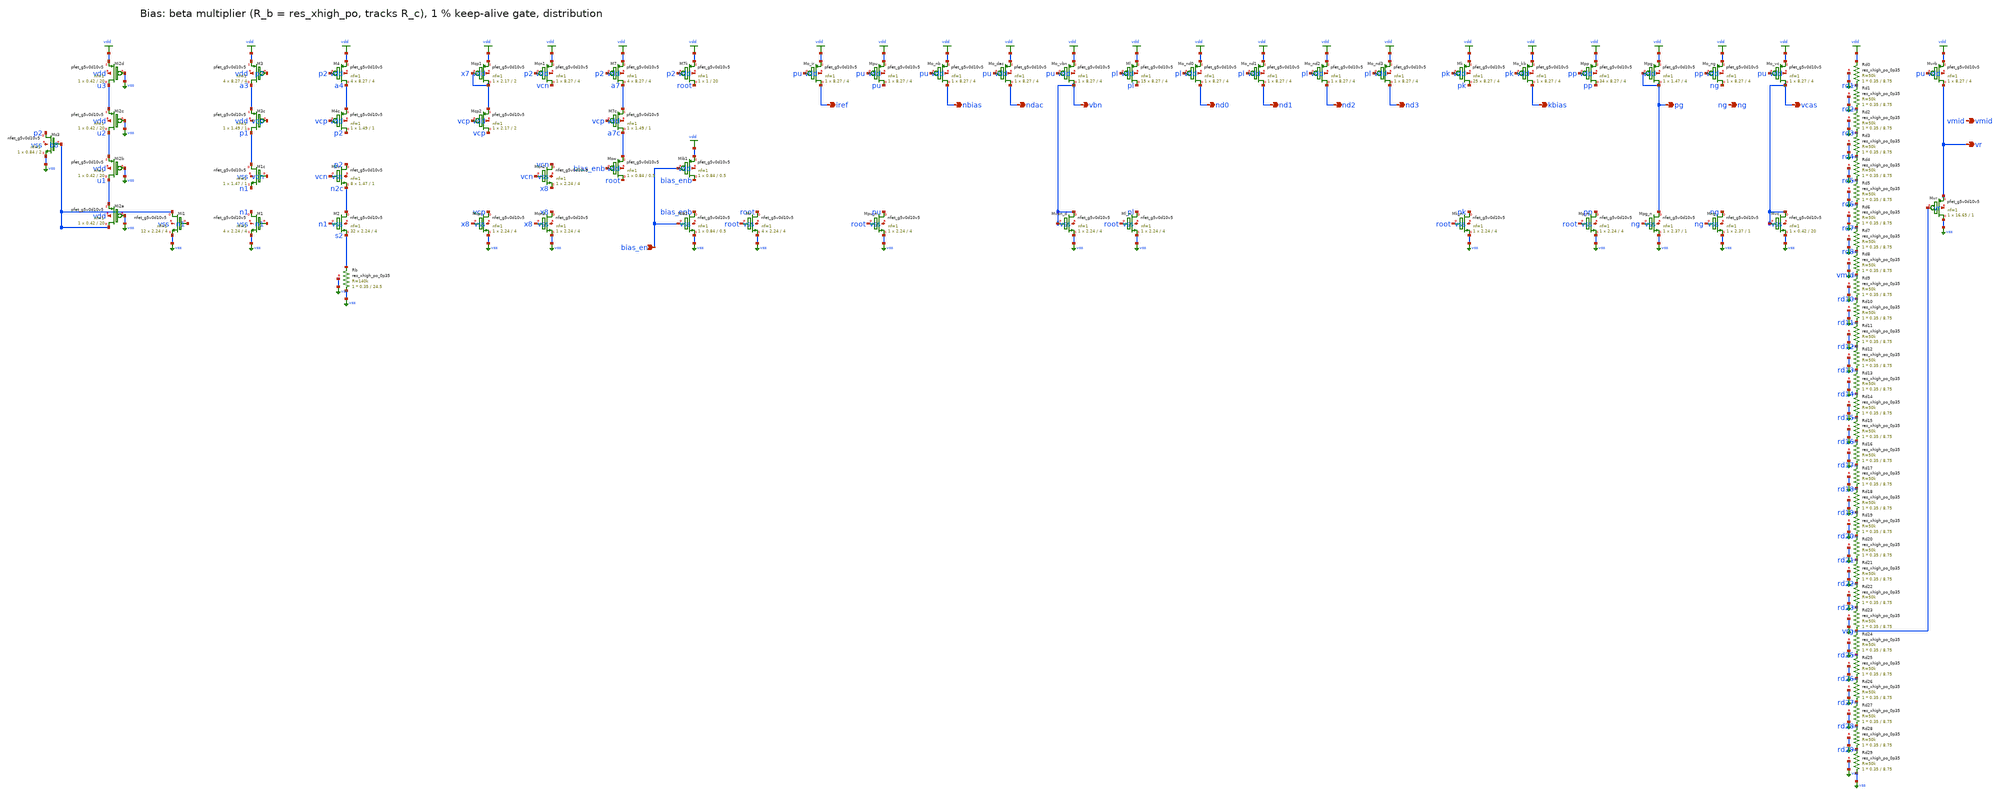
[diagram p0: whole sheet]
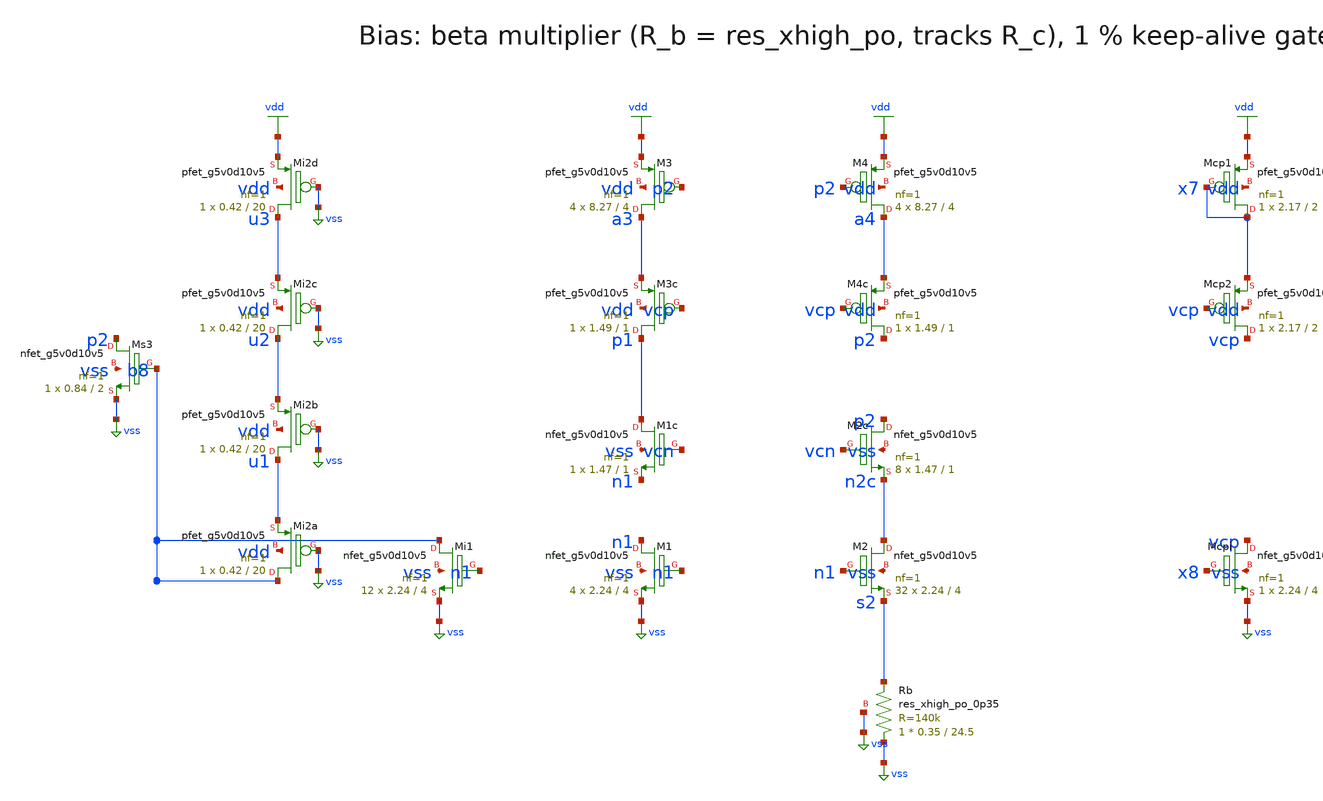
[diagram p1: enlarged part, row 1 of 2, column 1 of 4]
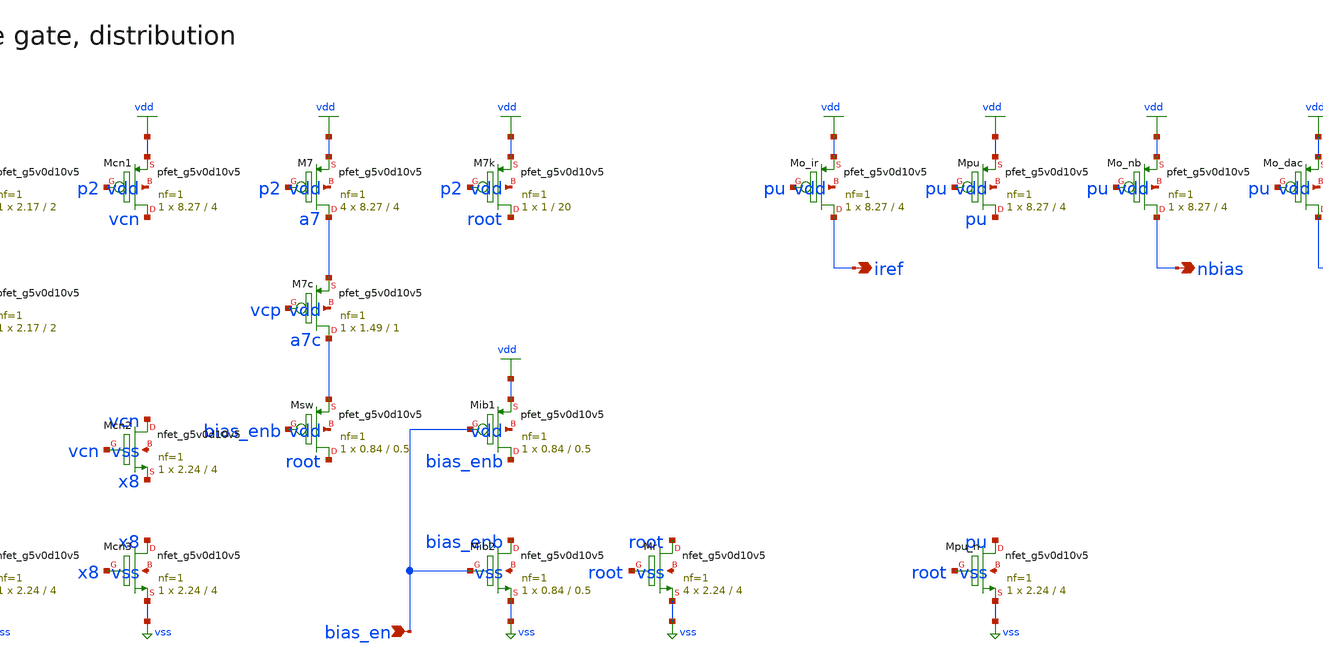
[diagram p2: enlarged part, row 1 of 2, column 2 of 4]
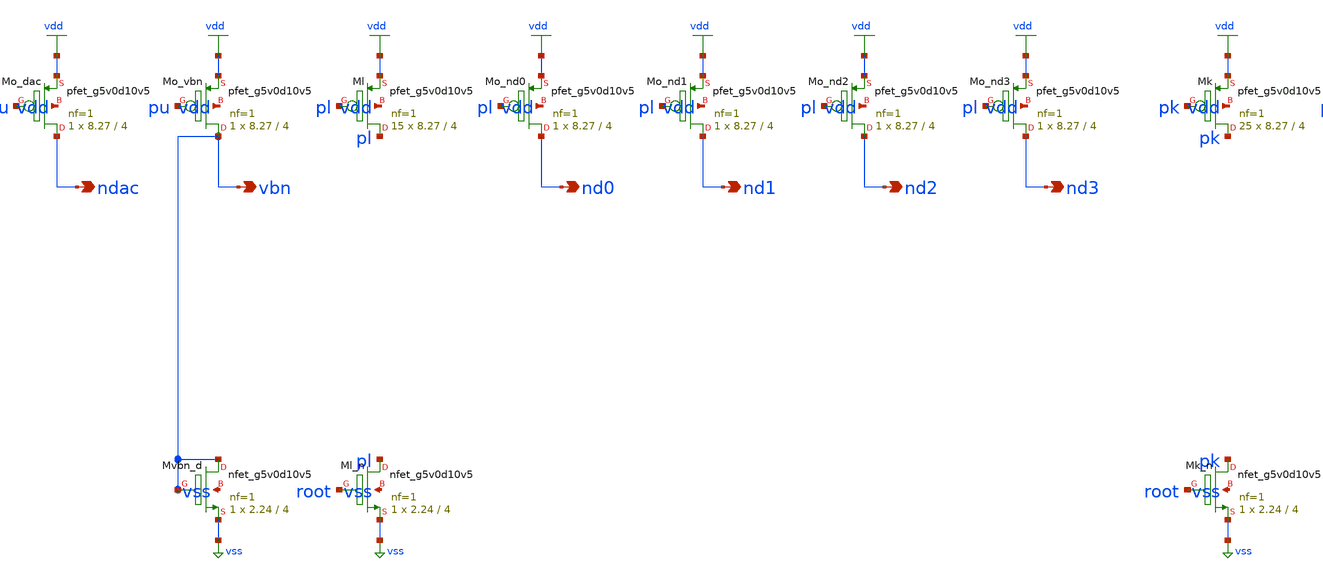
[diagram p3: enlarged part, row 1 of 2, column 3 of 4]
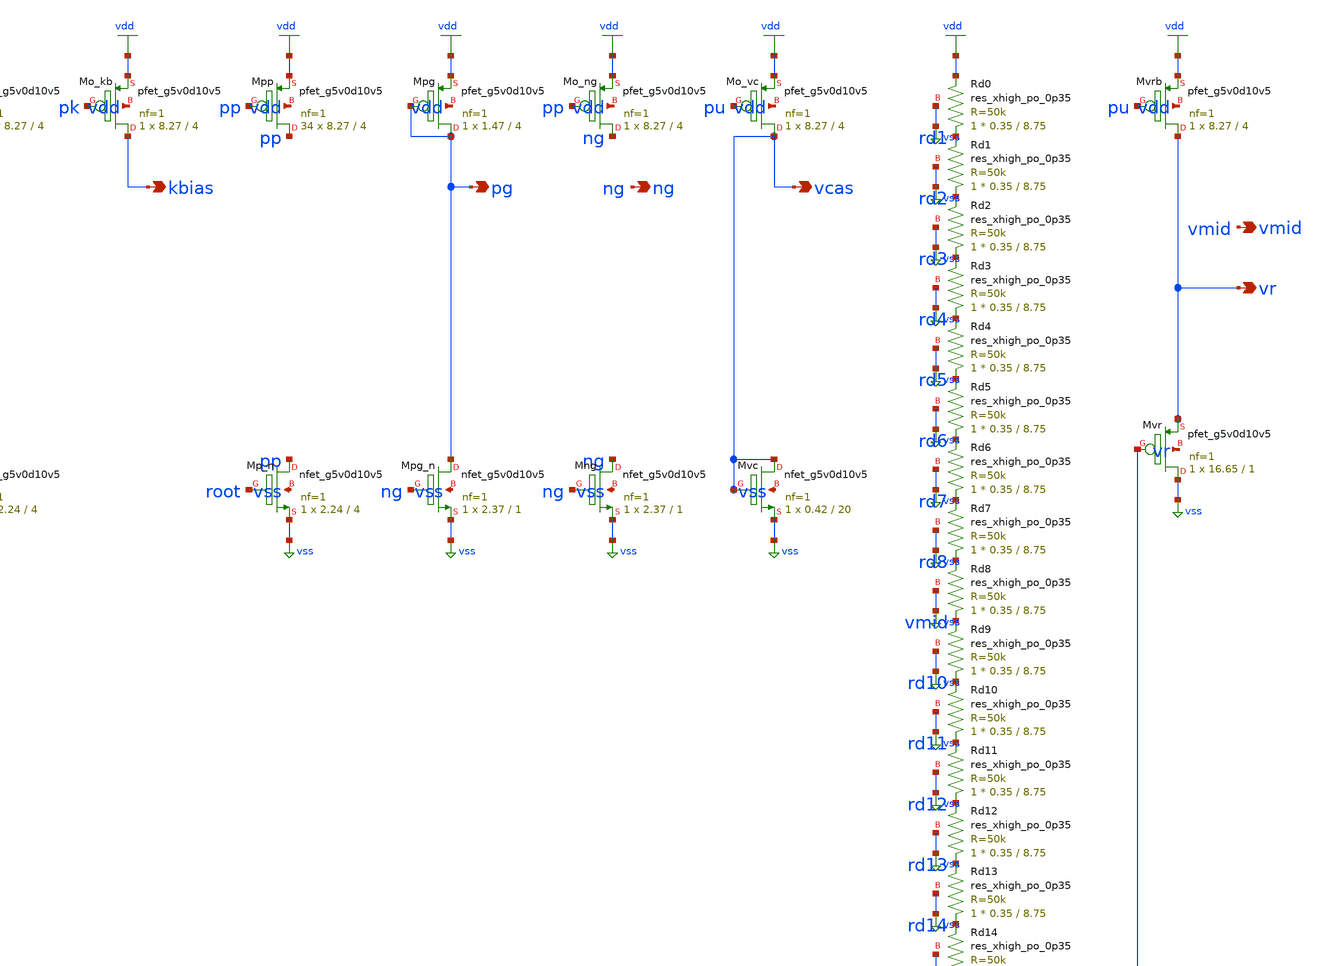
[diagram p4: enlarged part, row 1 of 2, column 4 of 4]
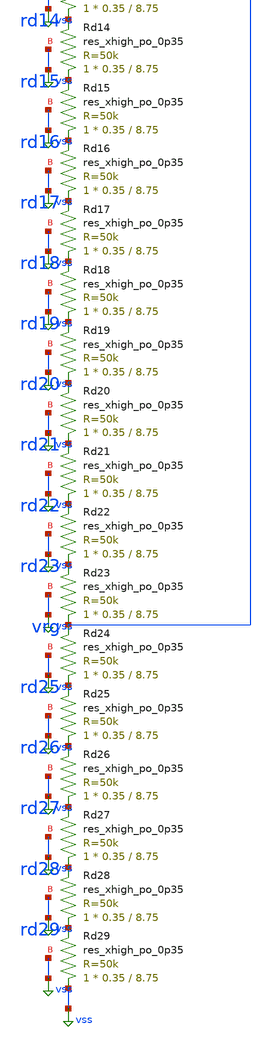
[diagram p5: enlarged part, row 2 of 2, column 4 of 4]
** sch_path: xschem/rt5w_bias.sch
**.subckt rt5w_bias bias_en nbias ndac vbn kbias pg ng vcas vr vmid iref nd0 nd1 nd2 nd3
*.ipin bias_en
*.opin nbias
*.opin ndac
*.opin vbn
*.opin kbias
*.opin pg
*.opin ng
*.opin vcas
*.opin vr
*.opin vmid
*.opin iref
*.opin nd0
*.opin nd1
*.opin nd2
*.opin nd3
XM1 n1 n1 vss vss sky130_fd_pr__nfet_g5v0d10v5 L=4 W=2.24 nf=1 ad=0.6496 as=0.6496 pd=5.06 ps=5.06
+ nrd=0.1295 nrs=0.1295 sa=0 sb=0 sd=0 mult=4 m=4
XM2 n2c n1 s2 vss sky130_fd_pr__nfet_g5v0d10v5 L=4 W=2.24 nf=1 ad=0.6496 as=0.6496 pd=5.06 ps=5.06
+ nrd=0.1295 nrs=0.1295 sa=0 sb=0 sd=0 mult=32 m=32
XRb vss s2 vss sky130_fd_pr__res_xhigh_po_0p35 L=24.5 mult=1 m=1
XM1c p1 vcn n1 vss sky130_fd_pr__nfet_g5v0d10v5 L=1 W=1.47 nf=1 ad=0.4263 as=0.4263 pd=3.52 ps=3.52
+ nrd=0.1973 nrs=0.1973 sa=0 sb=0 sd=0 mult=1 m=1
XM2c p2 vcn n2c vss sky130_fd_pr__nfet_g5v0d10v5 L=1 W=1.47 nf=1 ad=0.4263 as=0.4263 pd=3.52 ps=3.52
+ nrd=0.1973 nrs=0.1973 sa=0 sb=0 sd=0 mult=8 m=8
XM3c p1 vcp a3 vdd sky130_fd_pr__pfet_g5v0d10v5 L=1 W=1.49 nf=1 ad=0.4321 as=0.4321 pd=3.56 ps=3.56
+ nrd=0.1946 nrs=0.1946 sa=0 sb=0 sd=0 mult=1 m=1
XM4c p2 vcp a4 vdd sky130_fd_pr__pfet_g5v0d10v5 L=1 W=1.49 nf=1 ad=0.4321 as=0.4321 pd=3.56 ps=3.56
+ nrd=0.1946 nrs=0.1946 sa=0 sb=0 sd=0 mult=1 m=1
XM3 a3 p2 vdd vdd sky130_fd_pr__pfet_g5v0d10v5 L=4 W=8.27 nf=1 ad=2.398 as=2.398 pd=17.12 ps=17.12
+ nrd=0.03507 nrs=0.03507 sa=0 sb=0 sd=0 mult=4 m=4
XM4 a4 p2 vdd vdd sky130_fd_pr__pfet_g5v0d10v5 L=4 W=8.27 nf=1 ad=2.398 as=2.398 pd=17.12 ps=17.12
+ nrd=0.03507 nrs=0.03507 sa=0 sb=0 sd=0 mult=4 m=4
XMcp1 x7 x7 vdd vdd sky130_fd_pr__pfet_g5v0d10v5 L=2 W=2.17 nf=1 ad=0.6293 as=0.6293 pd=4.92 ps=4.92
+ nrd=0.1336 nrs=0.1336 sa=0 sb=0 sd=0 mult=1 m=1
XMcp2 vcp vcp x7 vdd sky130_fd_pr__pfet_g5v0d10v5 L=2 W=2.17 nf=1 ad=0.6293 as=0.6293 pd=4.92
+ ps=4.92 nrd=0.1336 nrs=0.1336 sa=0 sb=0 sd=0 mult=1 m=1
XMcpi vcp x8 vss vss sky130_fd_pr__nfet_g5v0d10v5 L=4 W=2.24 nf=1 ad=0.6496 as=0.6496 pd=5.06
+ ps=5.06 nrd=0.1295 nrs=0.1295 sa=0 sb=0 sd=0 mult=1 m=1
XMcn1 vcn p2 vdd vdd sky130_fd_pr__pfet_g5v0d10v5 L=4 W=8.27 nf=1 ad=2.398 as=2.398 pd=17.12
+ ps=17.12 nrd=0.03507 nrs=0.03507 sa=0 sb=0 sd=0 mult=1 m=1
XMcn2 vcn vcn x8 vss sky130_fd_pr__nfet_g5v0d10v5 L=4 W=2.24 nf=1 ad=0.6496 as=0.6496 pd=5.06
+ ps=5.06 nrd=0.1295 nrs=0.1295 sa=0 sb=0 sd=0 mult=1 m=1
XMcn3 x8 x8 vss vss sky130_fd_pr__nfet_g5v0d10v5 L=4 W=2.24 nf=1 ad=0.6496 as=0.6496 pd=5.06 ps=5.06
+ nrd=0.1295 nrs=0.1295 sa=0 sb=0 sd=0 mult=1 m=1
XMi1 b8 n1 vss vss sky130_fd_pr__nfet_g5v0d10v5 L=4 W=2.24 nf=1 ad=0.6496 as=0.6496 pd=5.06 ps=5.06
+ nrd=0.1295 nrs=0.1295 sa=0 sb=0 sd=0 mult=12 m=12
XMi2a b8 vss u1 vdd sky130_fd_pr__pfet_g5v0d10v5 L=20 W=0.42 nf=1 ad=0.1218 as=0.1218 pd=1.42
+ ps=1.42 nrd=0.6905 nrs=0.6905 sa=0 sb=0 sd=0 mult=1 m=1
XMi2b u1 vss u2 vdd sky130_fd_pr__pfet_g5v0d10v5 L=20 W=0.42 nf=1 ad=0.1218 as=0.1218 pd=1.42
+ ps=1.42 nrd=0.6905 nrs=0.6905 sa=0 sb=0 sd=0 mult=1 m=1
XMi2c u2 vss u3 vdd sky130_fd_pr__pfet_g5v0d10v5 L=20 W=0.42 nf=1 ad=0.1218 as=0.1218 pd=1.42
+ ps=1.42 nrd=0.6905 nrs=0.6905 sa=0 sb=0 sd=0 mult=1 m=1
XMi2d u3 vss vdd vdd sky130_fd_pr__pfet_g5v0d10v5 L=20 W=0.42 nf=1 ad=0.1218 as=0.1218 pd=1.42
+ ps=1.42 nrd=0.6905 nrs=0.6905 sa=0 sb=0 sd=0 mult=1 m=1
XMs3 p2 b8 vss vss sky130_fd_pr__nfet_g5v0d10v5 L=2 W=0.84 nf=1 ad=0.2436 as=0.2436 pd=2.26 ps=2.26
+ nrd=0.3452 nrs=0.3452 sa=0 sb=0 sd=0 mult=1 m=1
XM7 a7 p2 vdd vdd sky130_fd_pr__pfet_g5v0d10v5 L=4 W=8.27 nf=1 ad=2.398 as=2.398 pd=17.12 ps=17.12
+ nrd=0.03507 nrs=0.03507 sa=0 sb=0 sd=0 mult=4 m=4
XM7c a7c vcp a7 vdd sky130_fd_pr__pfet_g5v0d10v5 L=1 W=1.49 nf=1 ad=0.4321 as=0.4321 pd=3.56 ps=3.56
+ nrd=0.1946 nrs=0.1946 sa=0 sb=0 sd=0 mult=1 m=1
XMsw root bias_enb a7c vdd sky130_fd_pr__pfet_g5v0d10v5 L=0.5 W=0.84 nf=1 ad=0.2436 as=0.2436
+ pd=2.26 ps=2.26 nrd=0.3452 nrs=0.3452 sa=0 sb=0 sd=0 mult=1 m=1
XM7k root p2 vdd vdd sky130_fd_pr__pfet_g5v0d10v5 L=20 W=1 nf=1 ad=0.29 as=0.29 pd=2.58 ps=2.58
+ nrd=0.29 nrs=0.29 sa=0 sb=0 sd=0 mult=1 m=1
XMib1 bias_enb bias_en vdd vdd sky130_fd_pr__pfet_g5v0d10v5 L=0.5 W=0.84 nf=1 ad=0.2436 as=0.2436
+ pd=2.26 ps=2.26 nrd=0.3452 nrs=0.3452 sa=0 sb=0 sd=0 mult=1 m=1
XMib2 bias_enb bias_en vss vss sky130_fd_pr__nfet_g5v0d10v5 L=0.5 W=0.84 nf=1 ad=0.2436 as=0.2436
+ pd=2.26 ps=2.26 nrd=0.3452 nrs=0.3452 sa=0 sb=0 sd=0 mult=1 m=1
XMr root root vss vss sky130_fd_pr__nfet_g5v0d10v5 L=4 W=2.24 nf=1 ad=0.6496 as=0.6496 pd=5.06
+ ps=5.06 nrd=0.1295 nrs=0.1295 sa=0 sb=0 sd=0 mult=4 m=4
XMpu_n pu root vss vss sky130_fd_pr__nfet_g5v0d10v5 L=4 W=2.24 nf=1 ad=0.6496 as=0.6496 pd=5.06
+ ps=5.06 nrd=0.1295 nrs=0.1295 sa=0 sb=0 sd=0 mult=1 m=1
XMpu pu pu vdd vdd sky130_fd_pr__pfet_g5v0d10v5 L=4 W=8.27 nf=1 ad=2.398 as=2.398 pd=17.12 ps=17.12
+ nrd=0.03507 nrs=0.03507 sa=0 sb=0 sd=0 mult=1 m=1
XMo_nb nbias pu vdd vdd sky130_fd_pr__pfet_g5v0d10v5 L=4 W=8.27 nf=1 ad=2.398 as=2.398 pd=17.12
+ ps=17.12 nrd=0.03507 nrs=0.03507 sa=0 sb=0 sd=0 mult=1 m=1
XMo_dac ndac pu vdd vdd sky130_fd_pr__pfet_g5v0d10v5 L=4 W=8.27 nf=1 ad=2.398 as=2.398 pd=17.12
+ ps=17.12 nrd=0.03507 nrs=0.03507 sa=0 sb=0 sd=0 mult=1 m=1
XMo_ir iref pu vdd vdd sky130_fd_pr__pfet_g5v0d10v5 L=4 W=8.27 nf=1 ad=2.398 as=2.398 pd=17.12
+ ps=17.12 nrd=0.03507 nrs=0.03507 sa=0 sb=0 sd=0 mult=1 m=1
XMo_vbn vbn pu vdd vdd sky130_fd_pr__pfet_g5v0d10v5 L=4 W=8.27 nf=1 ad=2.398 as=2.398 pd=17.12
+ ps=17.12 nrd=0.03507 nrs=0.03507 sa=0 sb=0 sd=0 mult=1 m=1
XMvbn_d vbn vbn vss vss sky130_fd_pr__nfet_g5v0d10v5 L=4 W=2.24 nf=1 ad=0.6496 as=0.6496 pd=5.06
+ ps=5.06 nrd=0.1295 nrs=0.1295 sa=0 sb=0 sd=0 mult=1 m=1
XMl_n pl root vss vss sky130_fd_pr__nfet_g5v0d10v5 L=4 W=2.24 nf=1 ad=0.6496 as=0.6496 pd=5.06
+ ps=5.06 nrd=0.1295 nrs=0.1295 sa=0 sb=0 sd=0 mult=1 m=1
XMl pl pl vdd vdd sky130_fd_pr__pfet_g5v0d10v5 L=4 W=8.27 nf=1 ad=2.398 as=2.398 pd=17.12 ps=17.12
+ nrd=0.03507 nrs=0.03507 sa=0 sb=0 sd=0 mult=15 m=15
XMo_nd0 nd0 pl vdd vdd sky130_fd_pr__pfet_g5v0d10v5 L=4 W=8.27 nf=1 ad=2.398 as=2.398 pd=17.12
+ ps=17.12 nrd=0.03507 nrs=0.03507 sa=0 sb=0 sd=0 mult=1 m=1
XMo_nd1 nd1 pl vdd vdd sky130_fd_pr__pfet_g5v0d10v5 L=4 W=8.27 nf=1 ad=2.398 as=2.398 pd=17.12
+ ps=17.12 nrd=0.03507 nrs=0.03507 sa=0 sb=0 sd=0 mult=1 m=1
XMo_nd2 nd2 pl vdd vdd sky130_fd_pr__pfet_g5v0d10v5 L=4 W=8.27 nf=1 ad=2.398 as=2.398 pd=17.12
+ ps=17.12 nrd=0.03507 nrs=0.03507 sa=0 sb=0 sd=0 mult=1 m=1
XMo_nd3 nd3 pl vdd vdd sky130_fd_pr__pfet_g5v0d10v5 L=4 W=8.27 nf=1 ad=2.398 as=2.398 pd=17.12
+ ps=17.12 nrd=0.03507 nrs=0.03507 sa=0 sb=0 sd=0 mult=1 m=1
XMk_n pk root vss vss sky130_fd_pr__nfet_g5v0d10v5 L=4 W=2.24 nf=1 ad=0.6496 as=0.6496 pd=5.06
+ ps=5.06 nrd=0.1295 nrs=0.1295 sa=0 sb=0 sd=0 mult=1 m=1
XMk pk pk vdd vdd sky130_fd_pr__pfet_g5v0d10v5 L=4 W=8.27 nf=1 ad=2.398 as=2.398 pd=17.12 ps=17.12
+ nrd=0.03507 nrs=0.03507 sa=0 sb=0 sd=0 mult=25 m=25
XMo_kb kbias pk vdd vdd sky130_fd_pr__pfet_g5v0d10v5 L=4 W=8.27 nf=1 ad=2.398 as=2.398 pd=17.12
+ ps=17.12 nrd=0.03507 nrs=0.03507 sa=0 sb=0 sd=0 mult=1 m=1
XMp_n pp root vss vss sky130_fd_pr__nfet_g5v0d10v5 L=4 W=2.24 nf=1 ad=0.6496 as=0.6496 pd=5.06
+ ps=5.06 nrd=0.1295 nrs=0.1295 sa=0 sb=0 sd=0 mult=1 m=1
XMpp pp pp vdd vdd sky130_fd_pr__pfet_g5v0d10v5 L=4 W=8.27 nf=1 ad=2.398 as=2.398 pd=17.12 ps=17.12
+ nrd=0.03507 nrs=0.03507 sa=0 sb=0 sd=0 mult=34 m=34
XMpg pg pg vdd vdd sky130_fd_pr__pfet_g5v0d10v5 L=4 W=1.47 nf=1 ad=0.4263 as=0.4263 pd=3.52 ps=3.52
+ nrd=0.1973 nrs=0.1973 sa=0 sb=0 sd=0 mult=1 m=1
XMo_ng ng pp vdd vdd sky130_fd_pr__pfet_g5v0d10v5 L=4 W=8.27 nf=1 ad=2.398 as=2.398 pd=17.12
+ ps=17.12 nrd=0.03507 nrs=0.03507 sa=0 sb=0 sd=0 mult=1 m=1
XMng ng ng vss vss sky130_fd_pr__nfet_g5v0d10v5 L=1 W=2.37 nf=1 ad=0.6873 as=0.6873 pd=5.32 ps=5.32
+ nrd=0.1224 nrs=0.1224 sa=0 sb=0 sd=0 mult=1 m=1
XMpg_n pg ng vss vss sky130_fd_pr__nfet_g5v0d10v5 L=1 W=2.37 nf=1 ad=0.6873 as=0.6873 pd=5.32
+ ps=5.32 nrd=0.1224 nrs=0.1224 sa=0 sb=0 sd=0 mult=1 m=1
XMo_vc vcas pu vdd vdd sky130_fd_pr__pfet_g5v0d10v5 L=4 W=8.27 nf=1 ad=2.398 as=2.398 pd=17.12
+ ps=17.12 nrd=0.03507 nrs=0.03507 sa=0 sb=0 sd=0 mult=1 m=1
XMvc vcas vcas vss vss sky130_fd_pr__nfet_g5v0d10v5 L=20 W=0.42 nf=1 ad=0.1218 as=0.1218 pd=1.42
+ ps=1.42 nrd=0.6905 nrs=0.6905 sa=0 sb=0 sd=0 mult=1 m=1
XRd0 rd1 vdd vss sky130_fd_pr__res_xhigh_po_0p35 L=8.75 mult=1 m=1
XRd1 rd2 rd1 vss sky130_fd_pr__res_xhigh_po_0p35 L=8.75 mult=1 m=1
XRd2 rd3 rd2 vss sky130_fd_pr__res_xhigh_po_0p35 L=8.75 mult=1 m=1
XRd3 rd4 rd3 vss sky130_fd_pr__res_xhigh_po_0p35 L=8.75 mult=1 m=1
XRd4 rd5 rd4 vss sky130_fd_pr__res_xhigh_po_0p35 L=8.75 mult=1 m=1
XRd5 rd6 rd5 vss sky130_fd_pr__res_xhigh_po_0p35 L=8.75 mult=1 m=1
XRd6 rd7 rd6 vss sky130_fd_pr__res_xhigh_po_0p35 L=8.75 mult=1 m=1
XRd7 rd8 rd7 vss sky130_fd_pr__res_xhigh_po_0p35 L=8.75 mult=1 m=1
XRd8 vmid rd8 vss sky130_fd_pr__res_xhigh_po_0p35 L=8.75 mult=1 m=1
XRd9 rd10 vmid vss sky130_fd_pr__res_xhigh_po_0p35 L=8.75 mult=1 m=1
XRd10 rd11 rd10 vss sky130_fd_pr__res_xhigh_po_0p35 L=8.75 mult=1 m=1
XRd11 rd12 rd11 vss sky130_fd_pr__res_xhigh_po_0p35 L=8.75 mult=1 m=1
XRd12 rd13 rd12 vss sky130_fd_pr__res_xhigh_po_0p35 L=8.75 mult=1 m=1
XRd13 rd14 rd13 vss sky130_fd_pr__res_xhigh_po_0p35 L=8.75 mult=1 m=1
XRd14 rd15 rd14 vss sky130_fd_pr__res_xhigh_po_0p35 L=8.75 mult=1 m=1
XRd15 rd16 rd15 vss sky130_fd_pr__res_xhigh_po_0p35 L=8.75 mult=1 m=1
XRd16 rd17 rd16 vss sky130_fd_pr__res_xhigh_po_0p35 L=8.75 mult=1 m=1
XRd17 rd18 rd17 vss sky130_fd_pr__res_xhigh_po_0p35 L=8.75 mult=1 m=1
XRd18 rd19 rd18 vss sky130_fd_pr__res_xhigh_po_0p35 L=8.75 mult=1 m=1
XRd19 rd20 rd19 vss sky130_fd_pr__res_xhigh_po_0p35 L=8.75 mult=1 m=1
XRd20 rd21 rd20 vss sky130_fd_pr__res_xhigh_po_0p35 L=8.75 mult=1 m=1
XRd21 rd22 rd21 vss sky130_fd_pr__res_xhigh_po_0p35 L=8.75 mult=1 m=1
XRd22 rd23 rd22 vss sky130_fd_pr__res_xhigh_po_0p35 L=8.75 mult=1 m=1
XRd23 vrg rd23 vss sky130_fd_pr__res_xhigh_po_0p35 L=8.75 mult=1 m=1
XRd24 rd25 vrg vss sky130_fd_pr__res_xhigh_po_0p35 L=8.75 mult=1 m=1
XRd25 rd26 rd25 vss sky130_fd_pr__res_xhigh_po_0p35 L=8.75 mult=1 m=1
XRd26 rd27 rd26 vss sky130_fd_pr__res_xhigh_po_0p35 L=8.75 mult=1 m=1
XRd27 rd28 rd27 vss sky130_fd_pr__res_xhigh_po_0p35 L=8.75 mult=1 m=1
XRd28 rd29 rd28 vss sky130_fd_pr__res_xhigh_po_0p35 L=8.75 mult=1 m=1
XRd29 vss rd29 vss sky130_fd_pr__res_xhigh_po_0p35 L=8.75 mult=1 m=1
XMvr vss vrg vr vr sky130_fd_pr__pfet_g5v0d10v5 L=1 W=16.65 nf=1 ad=4.828 as=4.828 pd=33.88 ps=33.88
+ nrd=0.01742 nrs=0.01742 sa=0 sb=0 sd=0 mult=1 m=1
XMvrb vr pu vdd vdd sky130_fd_pr__pfet_g5v0d10v5 L=4 W=8.27 nf=1 ad=2.398 as=2.398 pd=17.12 ps=17.12
+ nrd=0.03507 nrs=0.03507 sa=0 sb=0 sd=0 mult=1 m=1
**.ends
.GLOBAL vdd
.GLOBAL vss
.end
